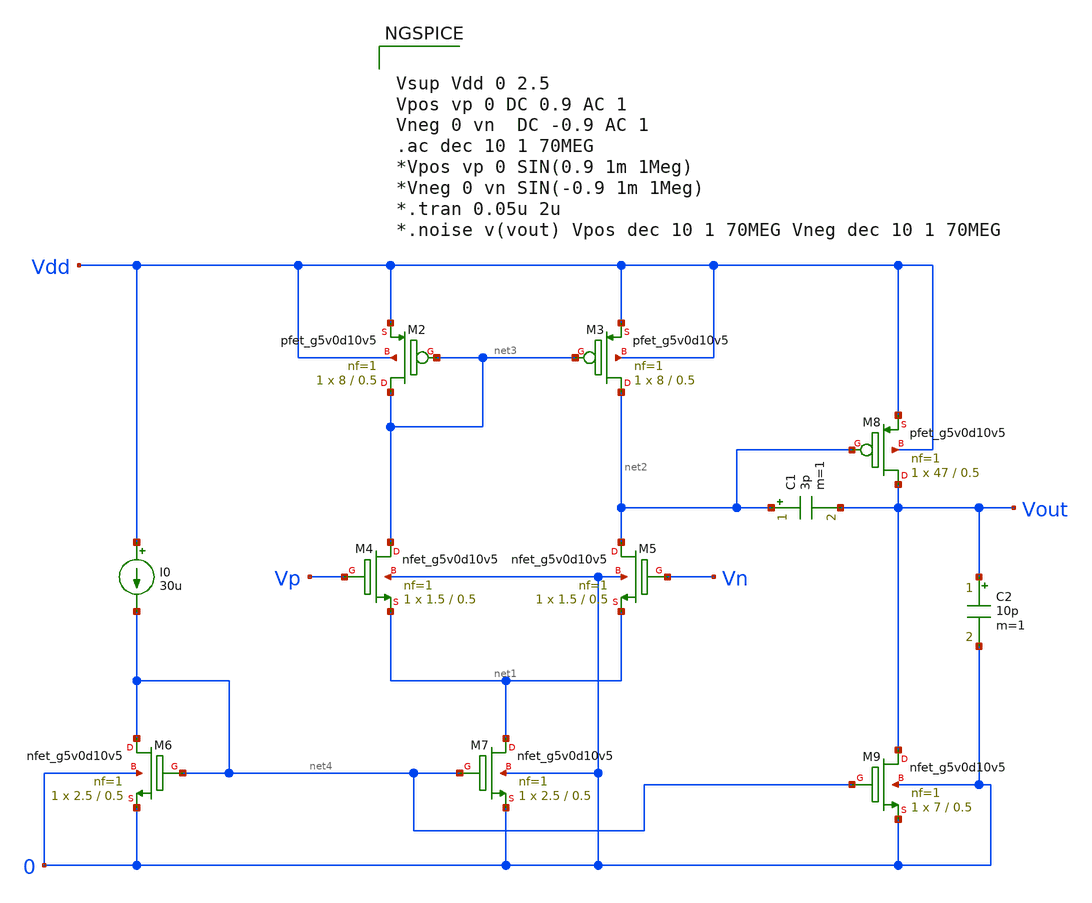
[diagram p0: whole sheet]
** sch_path: OTA/Schematic/LDO_OTA.sch
**.subckt LDO_OTA
I0 Vdd net4 30u
C1 net2 Vout 3p m=1
XM2 net3 net3 Vdd Vdd sky130_fd_pr__pfet_g5v0d10v5 L=0.5 W=8 nf=1 ad='int((nf+1)/2) * W/nf * 0.29' as='int((nf+2)/2) * W/nf * 0.29'
+ pd='2*int((nf+1)/2) * (W/nf + 0.29)' ps='2*int((nf+2)/2) * (W/nf + 0.29)' nrd='0.29 / W' nrs='0.29 / W'
+ sa=0 sb=0 sd=0 mult=1 m=1
XM3 net2 net3 Vdd Vdd sky130_fd_pr__pfet_g5v0d10v5 L=0.5 W=8 nf=1 ad='int((nf+1)/2) * W/nf * 0.29' as='int((nf+2)/2) * W/nf * 0.29'
+ pd='2*int((nf+1)/2) * (W/nf + 0.29)' ps='2*int((nf+2)/2) * (W/nf + 0.29)' nrd='0.29 / W' nrs='0.29 / W'
+ sa=0 sb=0 sd=0 mult=1 m=1
XM8 Vout net2 Vdd Vdd sky130_fd_pr__pfet_g5v0d10v5 L=0.5 W=47 nf=1 ad='int((nf+1)/2) * W/nf * 0.29' as='int((nf+2)/2) * W/nf * 0.29'
+ pd='2*int((nf+1)/2) * (W/nf + 0.29)' ps='2*int((nf+2)/2) * (W/nf + 0.29)' nrd='0.29 / W' nrs='0.29 / W'
+ sa=0 sb=0 sd=0 mult=1 m=1
XM5 net2 Vn net1 0 sky130_fd_pr__nfet_g5v0d10v5 L=0.5 W=1.5 nf=1 ad='int((nf+1)/2) * W/nf * 0.29' as='int((nf+2)/2) * W/nf * 0.29'
+ pd='2*int((nf+1)/2) * (W/nf + 0.29)' ps='2*int((nf+2)/2) * (W/nf + 0.29)' nrd='0.29 / W' nrs='0.29 / W'
+ sa=0 sb=0 sd=0 mult=1 m=1
XM4 net3 Vp net1 0 sky130_fd_pr__nfet_g5v0d10v5 L=0.5 W=1.5 nf=1 ad='int((nf+1)/2) * W/nf * 0.29' as='int((nf+2)/2) * W/nf * 0.29'
+ pd='2*int((nf+1)/2) * (W/nf + 0.29)' ps='2*int((nf+2)/2) * (W/nf + 0.29)' nrd='0.29 / W' nrs='0.29 / W'
+ sa=0 sb=0 sd=0 mult=1 m=1
XM7 net1 net4 0 0 sky130_fd_pr__nfet_g5v0d10v5 L=0.5 W=2.5 nf=1 ad='int((nf+1)/2) * W/nf * 0.29' as='int((nf+2)/2) * W/nf * 0.29'
+ pd='2*int((nf+1)/2) * (W/nf + 0.29)' ps='2*int((nf+2)/2) * (W/nf + 0.29)' nrd='0.29 / W' nrs='0.29 / W'
+ sa=0 sb=0 sd=0 mult=1 m=1
XM6 net4 net4 0 0 sky130_fd_pr__nfet_g5v0d10v5 L=0.5 W=2.5 nf=1 ad='int((nf+1)/2) * W/nf * 0.29' as='int((nf+2)/2) * W/nf * 0.29'
+ pd='2*int((nf+1)/2) * (W/nf + 0.29)' ps='2*int((nf+2)/2) * (W/nf + 0.29)' nrd='0.29 / W' nrs='0.29 / W'
+ sa=0 sb=0 sd=0 mult=1 m=1
XM9 Vout net4 0 0 sky130_fd_pr__nfet_g5v0d10v5 L=0.5 W=7 nf=1 ad='int((nf+1)/2) * W/nf * 0.29' as='int((nf+2)/2) * W/nf * 0.29'
+ pd='2*int((nf+1)/2) * (W/nf + 0.29)' ps='2*int((nf+2)/2) * (W/nf + 0.29)' nrd='0.29 / W' nrs='0.29 / W'
+ sa=0 sb=0 sd=0 mult=1 m=1
C2 Vout 0 10p m=1
**** begin user architecture code

.include $::SKYWATER_MODELS/cells/nfet_01v8/sky130_fd_pr__nfet_01v8__tt.corner.spice
.include $::SKYWATER_MODELS/cells/nfet_01v8_lvt/sky130_fd_pr__nfet_01v8_lvt__tt.corner.spice
.include $::SKYWATER_MODELS/cells/pfet_01v8/sky130_fd_pr__pfet_01v8__tt.corner.spice
.include $::SKYWATER_MODELS/cells/nfet_03v3_nvt/sky130_fd_pr__nfet_03v3_nvt__tt.corner.spice
.include $::SKYWATER_MODELS/cells/nfet_05v0_nvt/sky130_fd_pr__nfet_05v0_nvt__tt.corner.spice
.include $::SKYWATER_MODELS/cells/esd_nfet_01v8/sky130_fd_pr__esd_nfet_01v8__tt.corner.spice
.include $::SKYWATER_MODELS/cells/pfet_01v8_lvt/sky130_fd_pr__pfet_01v8_lvt__tt.corner.spice
.include $::SKYWATER_MODELS/cells/pfet_01v8_hvt/sky130_fd_pr__pfet_01v8_hvt__tt.corner.spice
.include $::SKYWATER_MODELS/cells/esd_pfet_g5v0d10v5/sky130_fd_pr__esd_pfet_g5v0d10v5__tt.corner.spice
.include $::SKYWATER_MODELS/cells/pfet_g5v0d10v5/sky130_fd_pr__pfet_g5v0d10v5__tt.corner.spice
.include $::SKYWATER_MODELS/cells/pfet_g5v0d16v0/sky130_fd_pr__pfet_g5v0d16v0__tt.corner.spice
.include $::SKYWATER_MODELS/cells/nfet_g5v0d10v5/sky130_fd_pr__nfet_g5v0d10v5__tt.corner.spice
.include $::SKYWATER_MODELS/cells/nfet_g5v0d16v0/sky130_fd_pr__nfet_g5v0d16v0__tt_discrete.corner.spice
.include $::SKYWATER_MODELS/cells/esd_nfet_g5v0d10v5/sky130_fd_pr__esd_nfet_g5v0d10v5__tt.corner.spice
.include $::SKYWATER_MODELS/models/corners/tt/nonfet.spice
* Mismatch parameters
.include $::SKYWATER_MODELS/cells/nfet_01v8/sky130_fd_pr__nfet_01v8__mismatch.corner.spice
.include $::SKYWATER_MODELS/cells/pfet_01v8/sky130_fd_pr__pfet_01v8__mismatch.corner.spice
.include $::SKYWATER_MODELS/cells/nfet_01v8_lvt/sky130_fd_pr__nfet_01v8_lvt__mismatch.corner.spice
.include $::SKYWATER_MODELS/cells/pfet_01v8_lvt/sky130_fd_pr__pfet_01v8_lvt__mismatch.corner.spice
.include $::SKYWATER_MODELS/cells/pfet_01v8_hvt/sky130_fd_pr__pfet_01v8_hvt__mismatch.corner.spice
.include $::SKYWATER_MODELS/cells/nfet_g5v0d10v5/sky130_fd_pr__nfet_g5v0d10v5__mismatch.corner.spice
.include $::SKYWATER_MODELS/cells/pfet_g5v0d10v5/sky130_fd_pr__pfet_g5v0d10v5__mismatch.corner.spice
.include $::SKYWATER_MODELS/cells/nfet_05v0_nvt/sky130_fd_pr__nfet_05v0_nvt__mismatch.corner.spice
.include $::SKYWATER_MODELS/cells/nfet_03v3_nvt/sky130_fd_pr__nfet_03v3_nvt__mismatch.corner.spice
* Resistor$::SKYWATER_MODELS/Capacitor
.include $::SKYWATER_MODELS/models/r+c/res_typical__cap_typical.spice
.include $::SKYWATER_MODELS/models/r+c/res_typical__cap_typical__lin.spice
* Special cells
.include $::SKYWATER_MODELS/models/corners/tt/specialized_cells.spice
* All models
.include $::SKYWATER_MODELS/models/all.spice
* Corner
.include $::SKYWATER_MODELS/models/corners/tt/rf.spice



Vsup Vdd 0 2.5
Vpos vp 0 DC 0.9 AC 1
Vneg 0 vn  DC -0.9 AC 1
.ac dec 10 1 70MEG
*Vpos vp 0 SIN(0.9 1m 1Meg)
*Vneg 0 vn SIN(-0.9 1m 1Meg)
*.tran 0.05u 2u
*.noise v(vout) Vpos dec 10 1 70MEG Vneg dec 10 1 70MEG


**** end user architecture code
**.ends
.end
